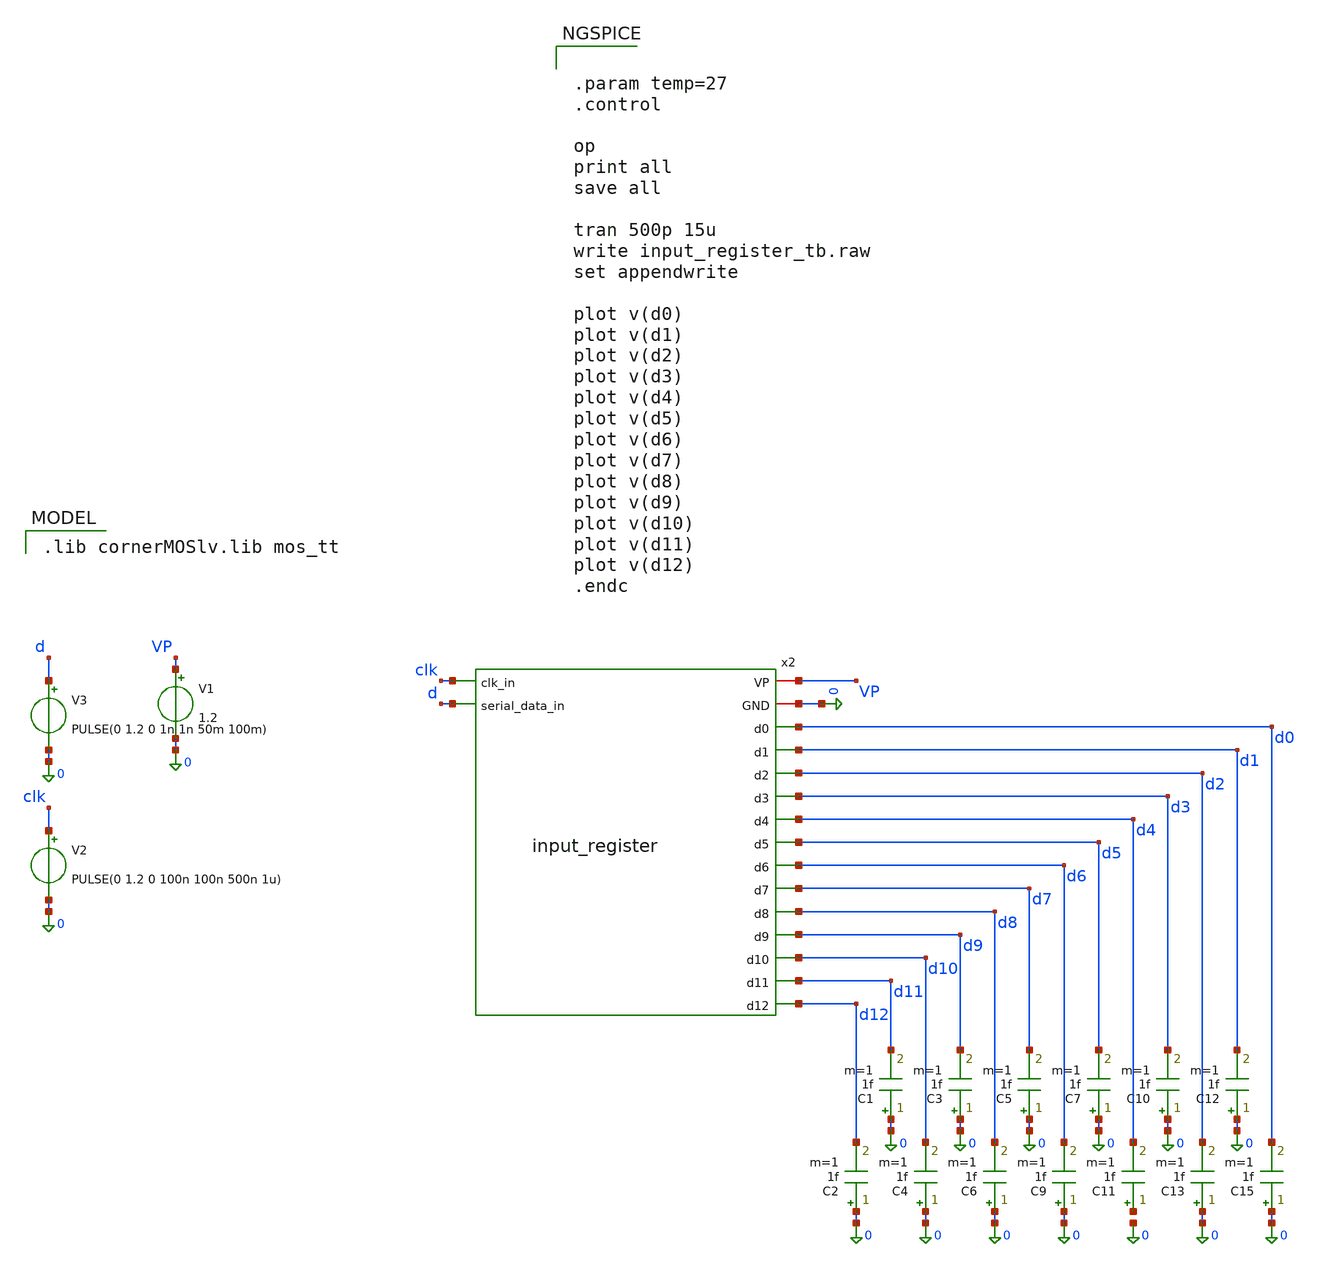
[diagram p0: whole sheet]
** sch_path: divider/tb/input_register_tb.sch
**.subckt input_register_tb
V1 VP 0 1.2
V2 clk 0 PULSE(0 1.2 0 100n 100n 500n 1u)
V3 d 0 PULSE(0 1.2 0 1n 1n 50m 100m)
C1 0 d11 1f m=1
C2 0 d12 1f m=1
C3 0 d9 1f m=1
C4 0 d10 1f m=1
C5 0 d7 1f m=1
C6 0 d8 1f m=1
C7 0 d5 1f m=1
C9 0 d6 1f m=1
C10 0 d3 1f m=1
C11 net1 d4 1f m=1
C12 0 d1 1f m=1
C13 0 d2 1f m=1
C15 0 d0 1f m=1
x2 VP 0 clk d2 d1 d0 d3 d d4 d7 d6 d5 d10 d9 d11 d8 d12 input_register
**** begin user architecture code
 .lib cornerMOSlv.lib mos_tt



.param temp=27
.control

op
print all
save all

tran 500p 15u
write input_register_tb.raw
set appendwrite

plot v(d0)
plot v(d1)
plot v(d2)
plot v(d3)
plot v(d4)
plot v(d5)
plot v(d6)
plot v(d7)
plot v(d8)
plot v(d9)
plot v(d10)
plot v(d11)
plot v(d12)
.endc


**** end user architecture code
**.ends
.end
